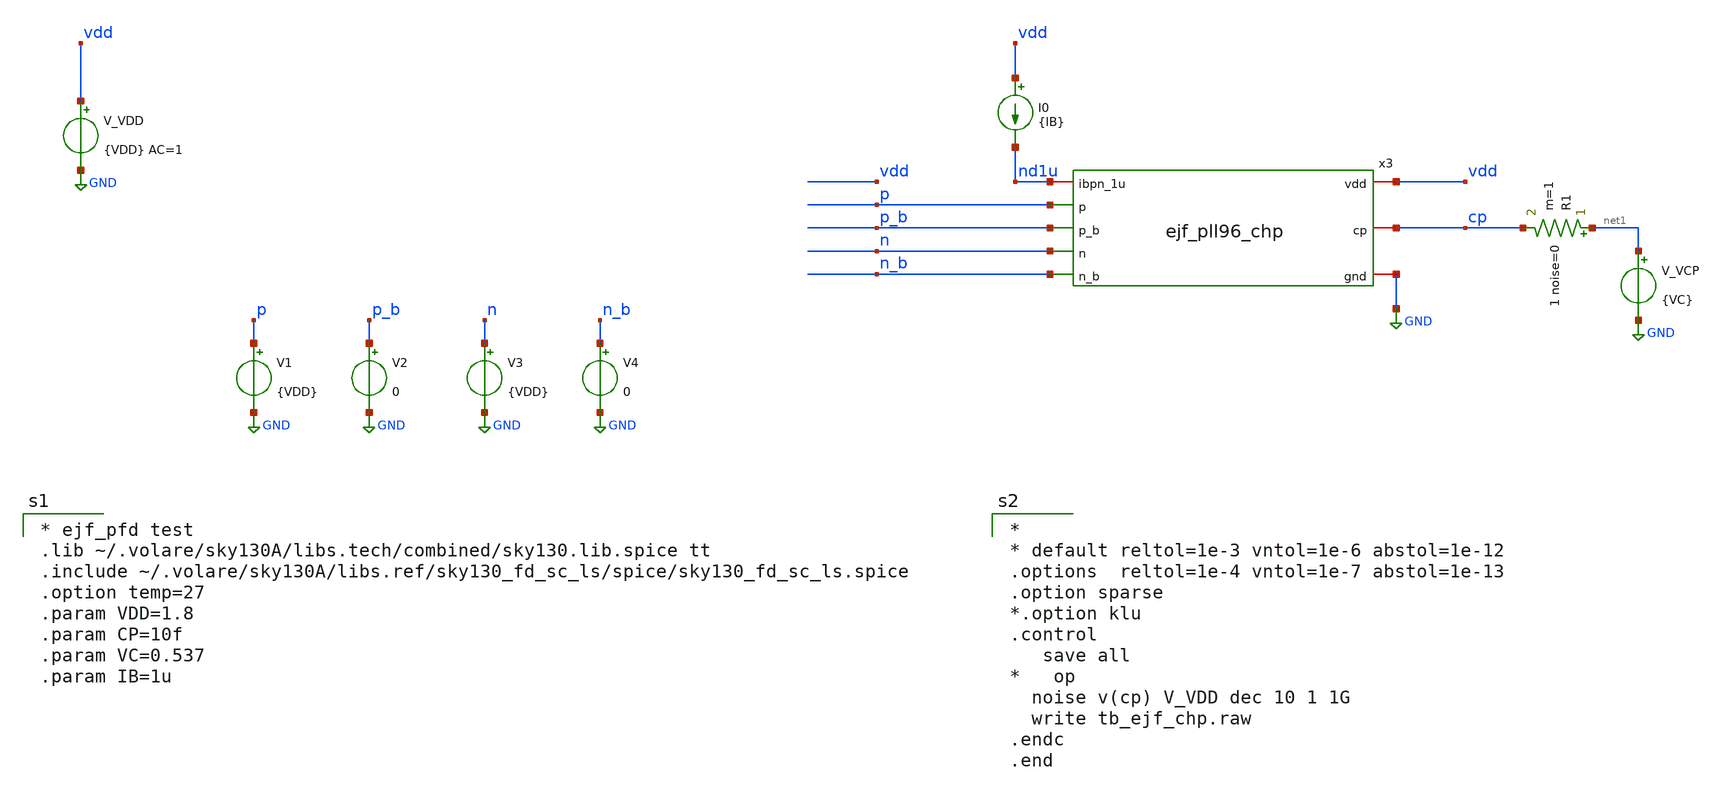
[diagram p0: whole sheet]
** sch_path: xschem/tb_ejf_pll96_chp.sch
**.subckt tb_ejf_pll96_chp
V_VDD vdd GND {VDD} AC=1
.save i(v_vdd)
x3 vdd p_b p cp nd1u n_b n GND ejf_pll96_chp
I0 vdd nd1u {IB}
V_VCP net1 GND {VC}
.save i(v_vcp)
V1 p GND {VDD}
.save i(v1)
V2 p_b GND 0
.save i(v2)
V3 n GND {VDD}
.save i(v3)
V4 n_b GND 0
.save i(v4)
R1 net1 cp 1 noise=0 m=1
**** begin user architecture code

* ejf_pfd test
.lib ~/.volare/sky130A/libs.tech/combined/sky130.lib.spice tt
.include ~/.volare/sky130A/libs.ref/sky130_fd_sc_ls/spice/sky130_fd_sc_ls.spice
.option temp=27
.param VDD=1.8
.param CP=10f
.param VC=0.537
.param IB=1u



*
* default reltol=1e-3 vntol=1e-6 abstol=1e-12
.options  reltol=1e-4 vntol=1e-7 abstol=1e-13
.option sparse
*.option klu
.control
   save all
*   op
  noise v(cp) V_VDD dec 10 1 1G
  write tb_ejf_chp.raw
.endc
.end

**** end user architecture code
**.ends

* expanding   symbol:  ejf_pll96_chp.sym # of pins=8
** sym_path: xschem/ejf_pll96_chp.sym
** sch_path: xschem/ejf_pll96_chp.sch
.subckt ejf_pll96_chp vdd p_b p cp ibpn_1u n_b n gnd
*.iopin vdd
*.iopin gnd
*.iopin ibpn_1u
*.iopin cp
*.ipin p
*.ipin n_b
*.ipin p_b
*.ipin n
XMN3 net1 mn1g gnd gnd sky130_fd_pr__nfet_01v8 L=0.5 W=1 nf=1 ad='int((nf+1)/2) * W/nf * 0.29' as='int((nf+2)/2) * W/nf * 0.29'
+ pd='2*int((nf+1)/2) * (W/nf + 0.29)' ps='2*int((nf+2)/2) * (W/nf + 0.29)' nrd='0.29 / W' nrs='0.29 / W'
+ sa=0 sb=0 sd=0 mult=1 m=1
XMN3C mn1g ibpn_1u net1 gnd sky130_fd_pr__nfet_01v8 L=0.15 W=1 nf=1 ad='int((nf+1)/2) * W/nf * 0.29'
+ as='int((nf+2)/2) * W/nf * 0.29' pd='2*int((nf+1)/2) * (W/nf + 0.29)' ps='2*int((nf+2)/2) * (W/nf + 0.29)'
+ nrd='0.29 / W' nrs='0.29 / W' sa=0 sb=0 sd=0 mult=1 m=1
XMP2 net2 mp1g vdd vdd sky130_fd_pr__pfet_01v8 L=0.5 W=2 nf=1 ad='int((nf+1)/2) * W/nf * 0.29' as='int((nf+2)/2) * W/nf * 0.29'
+ pd='2*int((nf+1)/2) * (W/nf + 0.29)' ps='2*int((nf+2)/2) * (W/nf + 0.29)' nrd='0.29 / W' nrs='0.29 / W'
+ sa=0 sb=0 sd=0 mult=1 m=1
XMN2 net3 mn1g gnd gnd sky130_fd_pr__nfet_01v8 L=0.5 W=1 nf=1 ad='int((nf+1)/2) * W/nf * 0.29' as='int((nf+2)/2) * W/nf * 0.29'
+ pd='2*int((nf+1)/2) * (W/nf + 0.29)' ps='2*int((nf+2)/2) * (W/nf + 0.29)' nrd='0.29 / W' nrs='0.29 / W'
+ sa=0 sb=0 sd=0 mult=1 m=1
XMN2C mp1cg ibpn_1u net3 gnd sky130_fd_pr__nfet_01v8 L=0.15 W=1 nf=1 ad='int((nf+1)/2) * W/nf * 0.29'
+ as='int((nf+2)/2) * W/nf * 0.29' pd='2*int((nf+1)/2) * (W/nf + 0.29)' ps='2*int((nf+2)/2) * (W/nf + 0.29)'
+ nrd='0.29 / W' nrs='0.29 / W' sa=0 sb=0 sd=0 mult=1 m=1
XMP1 mp1d mp1g vdd vdd sky130_fd_pr__pfet_01v8 L=0.5 W=2 nf=1 ad='int((nf+1)/2) * W/nf * 0.29' as='int((nf+2)/2) * W/nf * 0.29'
+ pd='2*int((nf+1)/2) * (W/nf + 0.29)' ps='2*int((nf+2)/2) * (W/nf + 0.29)' nrd='0.29 / W' nrs='0.29 / W'
+ sa=0 sb=0 sd=0 mult=5 m=5
XMP2C mp1g mp1cg net2 vdd sky130_fd_pr__pfet_01v8 L=0.15 W=2 nf=1 ad='int((nf+1)/2) * W/nf * 0.29' as='int((nf+2)/2) * W/nf * 0.29'
+ pd='2*int((nf+1)/2) * (W/nf + 0.29)' ps='2*int((nf+2)/2) * (W/nf + 0.29)' nrd='0.29 / W' nrs='0.29 / W'
+ sa=0 sb=0 sd=0 mult=1 m=1
XMP1C mp1cd mp1cg mp1d vdd sky130_fd_pr__pfet_01v8 L=0.15 W=2 nf=1 ad='int((nf+1)/2) * W/nf * 0.29' as='int((nf+2)/2) * W/nf * 0.29'
+ pd='2*int((nf+1)/2) * (W/nf + 0.29)' ps='2*int((nf+2)/2) * (W/nf + 0.29)' nrd='0.29 / W' nrs='0.29 / W'
+ sa=0 sb=0 sd=0 mult=5 m=5
XMN1 mn1d mn1g gnd gnd sky130_fd_pr__nfet_01v8 L=0.5 W=1 nf=1 ad='int((nf+1)/2) * W/nf * 0.29' as='int((nf+2)/2) * W/nf * 0.29'
+ pd='2*int((nf+1)/2) * (W/nf + 0.29)' ps='2*int((nf+2)/2) * (W/nf + 0.29)' nrd='0.29 / W' nrs='0.29 / W'
+ sa=0 sb=0 sd=0 mult=5 m=5
XM1C mn1cd ibpn_1u mn1d gnd sky130_fd_pr__nfet_01v8 L=0.15 W=1 nf=1 ad='int((nf+1)/2) * W/nf * 0.29'
+ as='int((nf+2)/2) * W/nf * 0.29' pd='2*int((nf+1)/2) * (W/nf + 0.29)' ps='2*int((nf+2)/2) * (W/nf + 0.29)'
+ nrd='0.29 / W' nrs='0.29 / W' sa=0 sb=0 sd=0 mult=5 m=5
XR1 mn1g net4 gnd sky130_fd_pr__res_xhigh_po W=0.35 L=10 mult=1 m=1
XR2 net4 ibpn_1u gnd sky130_fd_pr__res_xhigh_po W=0.35 L=10 mult=1 m=1
XR3 mp1cg net5 vdd sky130_fd_pr__res_xhigh_po W=0.35 L=10 mult=1 m=1
XR4 net5 mp1g vdd sky130_fd_pr__res_xhigh_po W=0.35 L=10 mult=1 m=1
XMP11 cp_replica p mp1cd vdd sky130_fd_pr__pfet_01v8 L=0.15 W=1 nf=1 ad='int((nf+1)/2) * W/nf * 0.29'
+ as='int((nf+2)/2) * W/nf * 0.29' pd='2*int((nf+1)/2) * (W/nf + 0.29)' ps='2*int((nf+2)/2) * (W/nf + 0.29)'
+ nrd='0.29 / W' nrs='0.29 / W' sa=0 sb=0 sd=0 mult=1 m=1
XMN11 cp_replica n_b mn1cd gnd sky130_fd_pr__nfet_01v8 L=0.15 W=1 nf=1 ad='int((nf+1)/2) * W/nf * 0.29'
+ as='int((nf+2)/2) * W/nf * 0.29' pd='2*int((nf+1)/2) * (W/nf + 0.29)' ps='2*int((nf+2)/2) * (W/nf + 0.29)'
+ nrd='0.29 / W' nrs='0.29 / W' sa=0 sb=0 sd=0 mult=1 m=1
XMP10 cp p_b mp1cd vdd sky130_fd_pr__pfet_01v8 L=0.15 W=1 nf=1 ad='int((nf+1)/2) * W/nf * 0.29' as='int((nf+2)/2) * W/nf * 0.29'
+ pd='2*int((nf+1)/2) * (W/nf + 0.29)' ps='2*int((nf+2)/2) * (W/nf + 0.29)' nrd='0.29 / W' nrs='0.29 / W'
+ sa=0 sb=0 sd=0 mult=1 m=1
XMN10 cp n mn1cd gnd sky130_fd_pr__nfet_01v8 L=0.15 W=1 nf=1 ad='int((nf+1)/2) * W/nf * 0.29' as='int((nf+2)/2) * W/nf * 0.29'
+ pd='2*int((nf+1)/2) * (W/nf + 0.29)' ps='2*int((nf+2)/2) * (W/nf + 0.29)' nrd='0.29 / W' nrs='0.29 / W'
+ sa=0 sb=0 sd=0 mult=1 m=1
XMN4CAP gnd mn1g gnd gnd sky130_fd_pr__nfet_01v8 L=0.5 W=1 nf=1 ad='int((nf+1)/2) * W/nf * 0.29' as='int((nf+2)/2) * W/nf * 0.29'
+ pd='2*int((nf+1)/2) * (W/nf + 0.29)' ps='2*int((nf+2)/2) * (W/nf + 0.29)' nrd='0.29 / W' nrs='0.29 / W'
+ sa=0 sb=0 sd=0 mult=7 m=7
XMP4CAP vdd mp1g vdd vdd sky130_fd_pr__pfet_01v8 L=0.5 W=2 nf=1 ad='int((nf+1)/2) * W/nf * 0.29' as='int((nf+2)/2) * W/nf * 0.29'
+ pd='2*int((nf+1)/2) * (W/nf + 0.29)' ps='2*int((nf+2)/2) * (W/nf + 0.29)' nrd='0.29 / W' nrs='0.29 / W'
+ sa=0 sb=0 sd=0 mult=6 m=6
XMP5CAP vdd mp1cg vdd vdd sky130_fd_pr__pfet_01v8 L=0.5 W=2 nf=1 ad='int((nf+1)/2) * W/nf * 0.29' as='int((nf+2)/2) * W/nf * 0.29'
+ pd='2*int((nf+1)/2) * (W/nf + 0.29)' ps='2*int((nf+2)/2) * (W/nf + 0.29)' nrd='0.29 / W' nrs='0.29 / W'
+ sa=0 sb=0 sd=0 mult=6 m=6
XMN5CAP gnd ibpn_1u gnd gnd sky130_fd_pr__nfet_01v8 L=0.5 W=1 nf=1 ad='int((nf+1)/2) * W/nf * 0.29' as='int((nf+2)/2) * W/nf * 0.29'
+ pd='2*int((nf+1)/2) * (W/nf + 0.29)' ps='2*int((nf+2)/2) * (W/nf + 0.29)' nrd='0.29 / W' nrs='0.29 / W'
+ sa=0 sb=0 sd=0 mult=7 m=7
XMP3 mp3d mp1g vdd vdd sky130_fd_pr__pfet_01v8 L=0.5 W=2 nf=1 ad='int((nf+1)/2) * W/nf * 0.29' as='int((nf+2)/2) * W/nf * 0.29'
+ pd='2*int((nf+1)/2) * (W/nf + 0.29)' ps='2*int((nf+2)/2) * (W/nf + 0.29)' nrd='0.29 / W' nrs='0.29 / W'
+ sa=0 sb=0 sd=0 mult=2 m=2
XMN6 cp_replica ibpn_1u net6 gnd sky130_fd_pr__nfet_01v8 L=0.15 W=1 nf=1 ad='int((nf+1)/2) * W/nf * 0.29'
+ as='int((nf+2)/2) * W/nf * 0.29' pd='2*int((nf+1)/2) * (W/nf + 0.29)' ps='2*int((nf+2)/2) * (W/nf + 0.29)'
+ nrd='0.29 / W' nrs='0.29 / W' sa=0 sb=0 sd=0 mult=1 m=1
XMN7 ng ibpn_1u net7 gnd sky130_fd_pr__nfet_01v8 L=0.15 W=1 nf=1 ad='int((nf+1)/2) * W/nf * 0.29' as='int((nf+2)/2) * W/nf * 0.29'
+ pd='2*int((nf+1)/2) * (W/nf + 0.29)' ps='2*int((nf+2)/2) * (W/nf + 0.29)' nrd='0.29 / W' nrs='0.29 / W'
+ sa=0 sb=0 sd=0 mult=1 m=1
XC2 cp_replica gnd sky130_fd_pr__cap_mim_m3_1 W=14 L=14 MF=1 m=1
XM1 cp_replica cp_replica mp3d VDD sky130_fd_pr__pfet_01v8_lvt L=0.35 W=4 nf=2 ad='int((nf+1)/2) * W/nf * 0.29'
+ as='int((nf+2)/2) * W/nf * 0.29' pd='2*int((nf+1)/2) * (W/nf + 0.29)' ps='2*int((nf+2)/2) * (W/nf + 0.29)'
+ nrd='0.29 / W' nrs='0.29 / W' sa=0 sb=0 sd=0 mult=1 m=1
XM2 ng cp mp3d VDD sky130_fd_pr__pfet_01v8_lvt L=0.35 W=4 nf=2 ad='int((nf+1)/2) * W/nf * 0.29' as='int((nf+2)/2) * W/nf * 0.29'
+ pd='2*int((nf+1)/2) * (W/nf + 0.29)' ps='2*int((nf+2)/2) * (W/nf + 0.29)' nrd='0.29 / W' nrs='0.29 / W'
+ sa=0 sb=0 sd=0 mult=1 m=1
XM3 net7 ng gnd GND sky130_fd_pr__nfet_01v8_lvt L=0.35 W=2 nf=2 ad='int((nf+1)/2) * W/nf * 0.29' as='int((nf+2)/2) * W/nf * 0.29'
+ pd='2*int((nf+1)/2) * (W/nf + 0.29)' ps='2*int((nf+2)/2) * (W/nf + 0.29)' nrd='0.29 / W' nrs='0.29 / W'
+ sa=0 sb=0 sd=0 mult=1 m=1
XM4 net6 ng gnd GND sky130_fd_pr__nfet_01v8_lvt L=0.35 W=2 nf=2 ad='int((nf+1)/2) * W/nf * 0.29' as='int((nf+2)/2) * W/nf * 0.29'
+ pd='2*int((nf+1)/2) * (W/nf + 0.29)' ps='2*int((nf+2)/2) * (W/nf + 0.29)' nrd='0.29 / W' nrs='0.29 / W'
+ sa=0 sb=0 sd=0 mult=1 m=1
C1 vdd mp1g 1u m=1
C3 vdd mp1cg 1u m=1
C4 ibpn_1u gnd 1u m=1
C5 ibpn_1u gnd 1u m=1
C6 cp_replica gnd 1u m=1
.ends

.GLOBAL GND
.end
